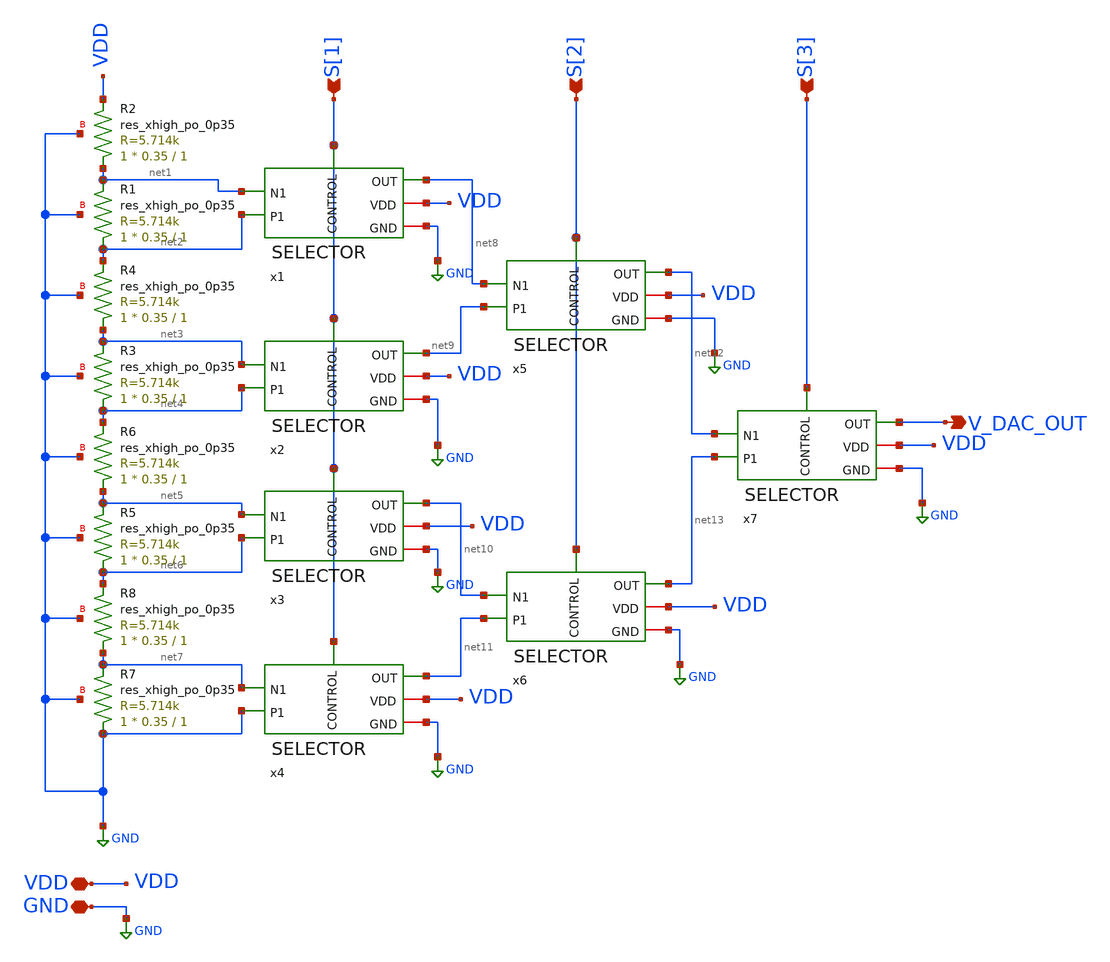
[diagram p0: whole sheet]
** sch_path: src/analog_source_files/DAC.sch
**.subckt DAC S[1] S[2] S[3] VDD GND V_DAC_OUT
*.ipin S[1]
*.ipin S[2]
*.ipin S[3]
*.iopin VDD
*.iopin GND
*.opin V_DAC_OUT
XR1 net2 net1 GND sky130_fd_pr__res_xhigh_po_0p35 L=1 mult=1 m=1
XR2 net1 VDD GND sky130_fd_pr__res_xhigh_po_0p35 L=1 mult=1 m=1
XR3 net4 net3 GND sky130_fd_pr__res_xhigh_po_0p35 L=1 mult=1 m=1
XR4 net3 net2 GND sky130_fd_pr__res_xhigh_po_0p35 L=1 mult=1 m=1
XR5 net6 net5 GND sky130_fd_pr__res_xhigh_po_0p35 L=1 mult=1 m=1
XR6 net5 net4 GND sky130_fd_pr__res_xhigh_po_0p35 L=1 mult=1 m=1
XR7 GND net7 GND sky130_fd_pr__res_xhigh_po_0p35 L=1 mult=1 m=1
XR8 net7 net6 GND sky130_fd_pr__res_xhigh_po_0p35 L=1 mult=1 m=1
x1 S[1] net1 net8 net2 VDD GND SELECTOR
x2 S[1] net3 net9 net4 VDD GND SELECTOR
x3 S[1] net5 net10 net6 VDD GND SELECTOR
x4 S[1] net7 net11 GND VDD GND SELECTOR
x5 S[2] net8 net12 net9 VDD GND SELECTOR
x6 S[2] net10 net13 net11 VDD GND SELECTOR
x7 S[3] net12 V_DAC_OUT net13 VDD GND SELECTOR
**.ends
.GLOBAL GND
.end
